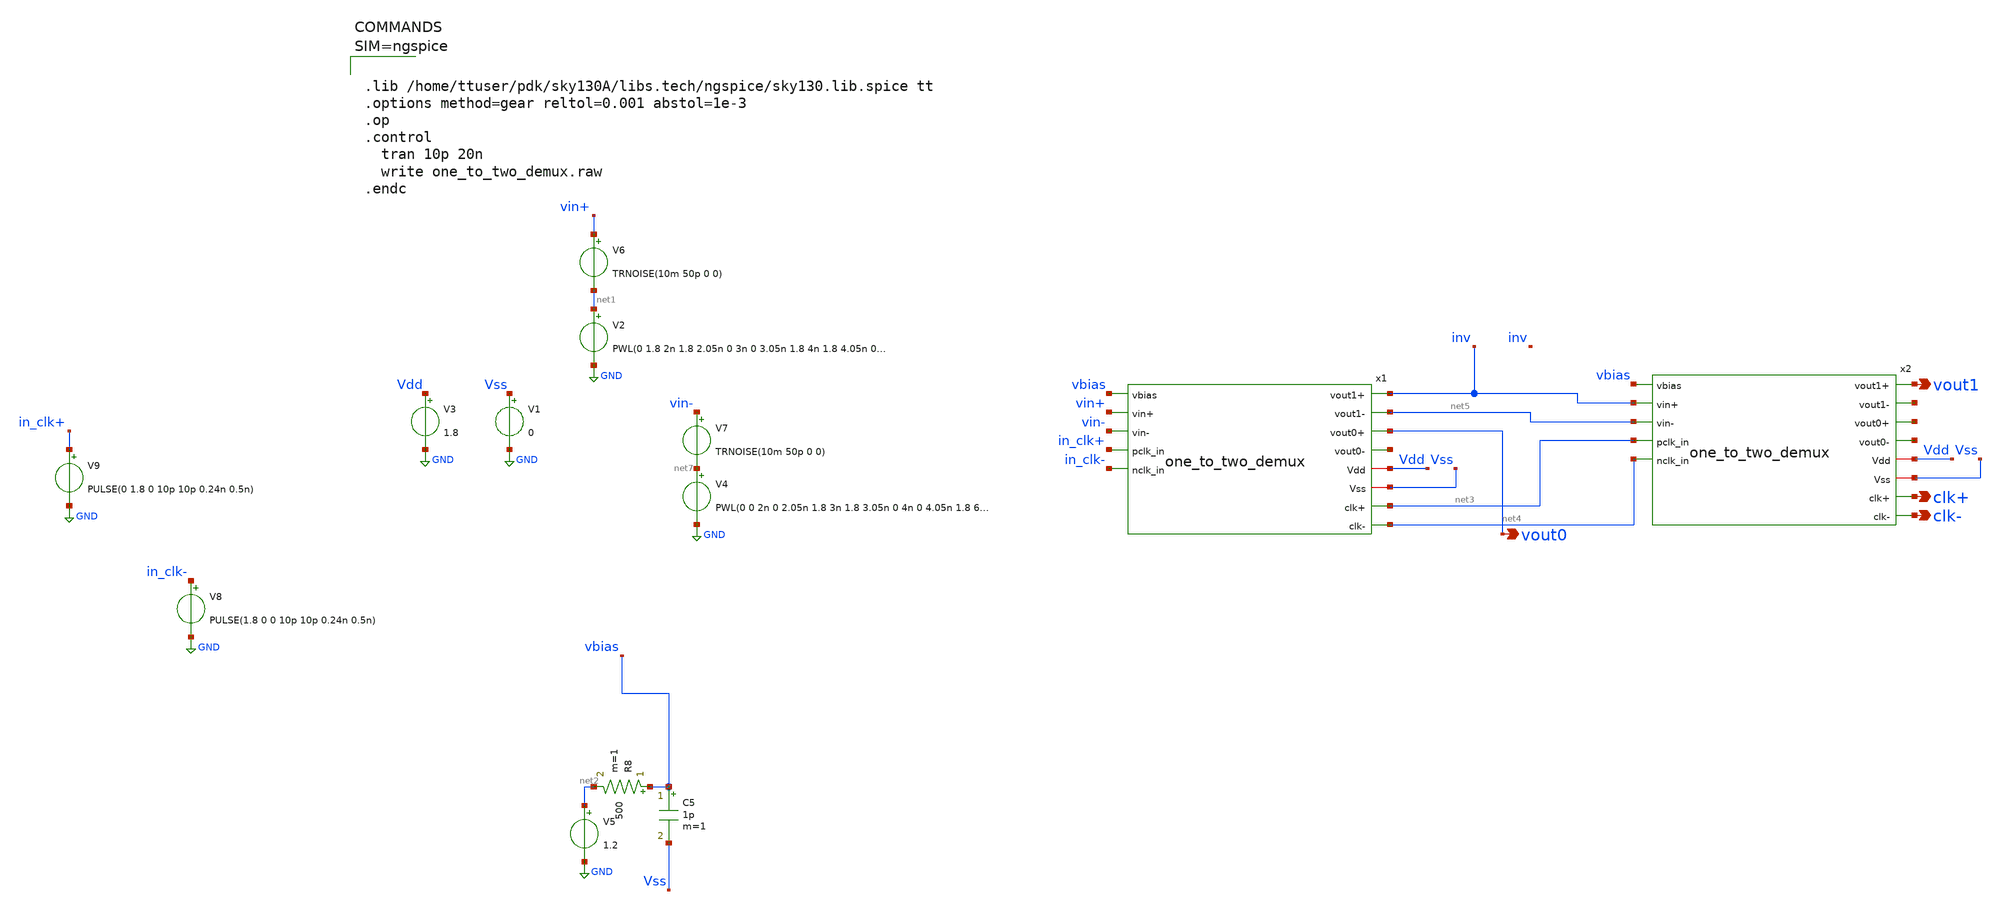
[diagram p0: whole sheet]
** sch_path: xschem/attic/one_two_demux_tb.sch
**.subckt one_two_demux_tb vout0 clk+ clk- vout1
*.opin vout0
*.opin clk+
*.opin clk-
*.opin vout1
x1 inv net5 vbias vin+ vout0 net6 vin- Vdd Vss in_clk+ net3 in_clk- net4 one_to_two_demux
V3 Vdd GND 1.8
V1 Vss GND 0
V2 net1 GND PWL(0 1.8 2n 1.8 2.05n 0 3n 0 3.05n 1.8 4n 1.8 4.05n 0 6n 0 6.05n 1.8 8n 1.8)
V4 net7 GND PWL(0 0 2n 0 2.05n 1.8 3n 1.8 3.05n 0 4n 0 4.05n 1.8 6n 1.8 6.05n 0 8n 0)
V5 net2 GND 1.2
V6 vin+ net1 TRNOISE(10m 50p 0 0)
V7 vin- net7 TRNOISE(10m 50p 0 0)
R8 vbias net2 500 m=1
C5 vbias Vss 1p m=1
V8 in_clk- GND PULSE(1.8 0 0 10p 10p 0.24n 0.5n)
V9 in_clk+ GND PULSE(0 1.8 0 10p 10p 0.24n 0.5n)
x2 vout1 net8 vbias inv net9 net10 net5 Vdd Vss net3 clk+ net4 clk- one_to_two_demux
**** begin user architecture code



.lib /home/ttuser/pdk/sky130A/libs.tech/ngspice/sky130.lib.spice tt
.options method=gear reltol=0.001 abstol=1e-3
.op
.control
  tran 10p 20n
  write one_to_two_demux.raw
.endc



**** end user architecture code
**.ends
.GLOBAL GND
.end
